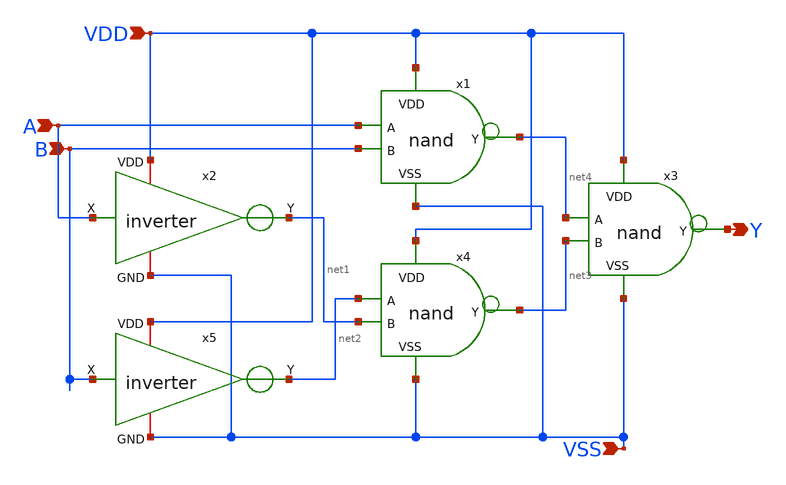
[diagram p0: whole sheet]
** sch_path: Layouts and Schematics/Spice Sim and Schem/xnor.sch
**.subckt xnor VDD VSS A B Y
*.ipin VDD
*.ipin VSS
*.ipin A
*.ipin B
*.opin Y
x1 VDD A net4 B VSS nand
x2 VDD A net1 VSS inv
x3 VDD net4 Y net3 VSS nand
x4 VDD net2 net3 net1 VSS nand
x5 VDD B net2 VSS inv
**.ends

* expanding   symbol:  nand.sym # of pins=5
** sym_path: Layouts and Schematics/Spice Sim and Schem/nand.sym
** sch_path: Layouts and Schematics/Spice Sim and Schem/nand.sch
.subckt nand VDD A Y B VSS
*.ipin A
*.ipin B
*.ipin VSS
*.opin Y
*.ipin VDD
XM1 Y B net1 VSS sky130_fd_pr__nfet_01v8 L=0.5 W=2 nf=1 ad='int((nf+1)/2) * W/nf * 0.29' as='int((nf+2)/2) * W/nf * 0.29'
+ pd='2*int((nf+1)/2) * (W/nf + 0.29)' ps='2*int((nf+2)/2) * (W/nf + 0.29)' nrd='0.29 / W' nrs='0.29 / W'
+ sa=0 sb=0 sd=0 mult=1 m=1
XM3 Y B VDD VDD sky130_fd_pr__pfet_01v8 L=0.5 W=2 nf=1 ad='int((nf+1)/2) * W/nf * 0.29' as='int((nf+2)/2) * W/nf * 0.29'
+ pd='2*int((nf+1)/2) * (W/nf + 0.29)' ps='2*int((nf+2)/2) * (W/nf + 0.29)' nrd='0.29 / W' nrs='0.29 / W'
+ sa=0 sb=0 sd=0 mult=1 m=1
XM4 Y A VDD VDD sky130_fd_pr__pfet_01v8 L=0.5 W=2 nf=1 ad='int((nf+1)/2) * W/nf * 0.29' as='int((nf+2)/2) * W/nf * 0.29'
+ pd='2*int((nf+1)/2) * (W/nf + 0.29)' ps='2*int((nf+2)/2) * (W/nf + 0.29)' nrd='0.29 / W' nrs='0.29 / W'
+ sa=0 sb=0 sd=0 mult=1 m=1
XM2 net1 A VSS VSS sky130_fd_pr__nfet_01v8 L=0.5 W=2 nf=1 ad='int((nf+1)/2) * W/nf * 0.29' as='int((nf+2)/2) * W/nf * 0.29'
+ pd='2*int((nf+1)/2) * (W/nf + 0.29)' ps='2*int((nf+2)/2) * (W/nf + 0.29)' nrd='0.29 / W' nrs='0.29 / W'
+ sa=0 sb=0 sd=0 mult=1 m=1
.ends


* expanding   symbol:  inv.sym # of pins=4
** sym_path: Layouts and Schematics/Spice Sim and Schem/inv.sym
** sch_path: Layouts and Schematics/Spice Sim and Schem/inv.sch
.subckt inv VDD X Y GND
*.ipin X
*.iopin VDD
*.iopin GND
*.opin Y
XM1 Y X GND GND sky130_fd_pr__nfet_01v8 L=0.5 W=1 nf=1 ad='int((nf+1)/2) * W/nf * 0.29' as='int((nf+2)/2) * W/nf * 0.29'
+ pd='2*int((nf+1)/2) * (W/nf + 0.29)' ps='2*int((nf+2)/2) * (W/nf + 0.29)' nrd='0.29 / W' nrs='0.29 / W'
+ sa=0 sb=0 sd=0 mult=1 m=1
XM2 Y X VDD VDD sky130_fd_pr__pfet_01v8 L=0.5 W=2 nf=1 ad='int((nf+1)/2) * W/nf * 0.29' as='int((nf+2)/2) * W/nf * 0.29'
+ pd='2*int((nf+1)/2) * (W/nf + 0.29)' ps='2*int((nf+2)/2) * (W/nf + 0.29)' nrd='0.29 / W' nrs='0.29 / W'
+ sa=0 sb=0 sd=0 mult=1 m=1
.ends

.end
